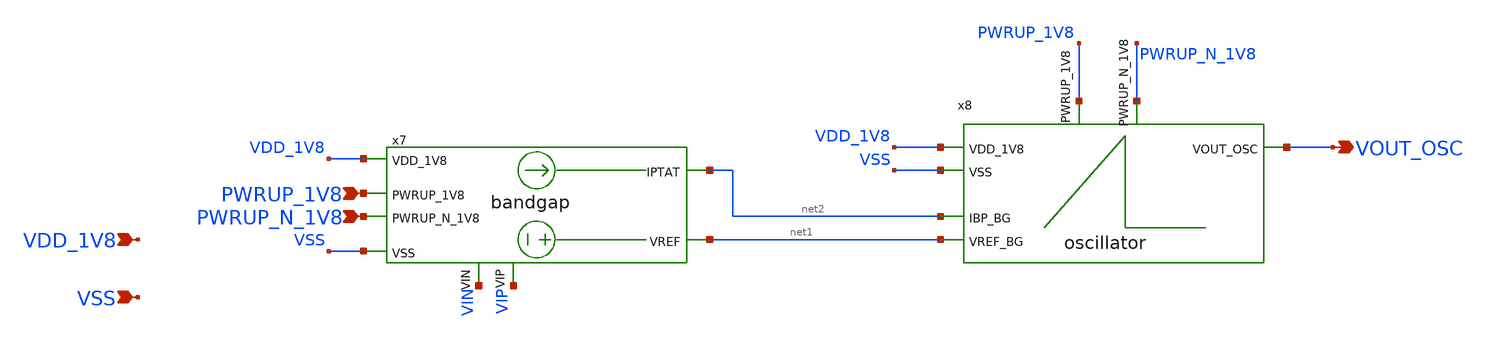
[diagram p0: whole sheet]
** sch_path: design/LELO_GR01_SKY130A/oscillator_tb.sch
**.subckt oscillator_tb VSS VDD_1V8 VOUT_OSC PWRUP_1V8 PWRUP_N_1V8
*.ipin VSS
*.ipin VDD_1V8
*.opin VOUT_OSC
*.ipin PWRUP_1V8
*.ipin PWRUP_N_1V8
x7 net2 net1 PWRUP_1V8 VDD_1V8 VSS PWRUP_N_1V8 VIN VIP bandgap
x8 VOUT_OSC VDD_1V8 VSS net2 net1 PWRUP_1V8 PWRUP_N_1V8 oscillator
**.ends
.end
